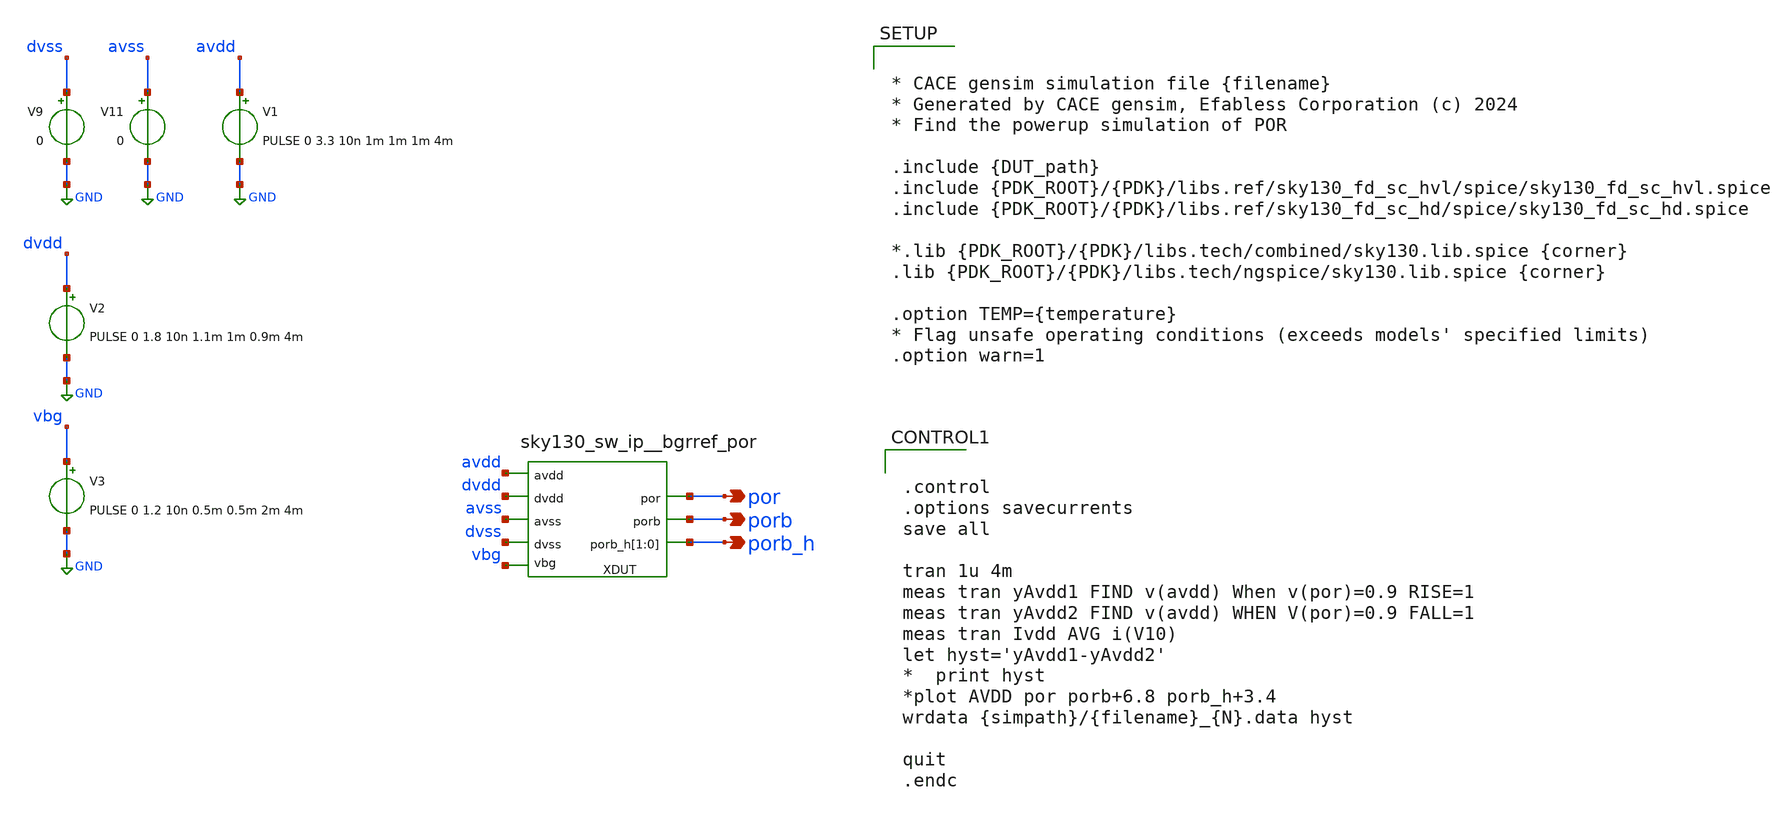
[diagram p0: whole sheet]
** sch_path: cace/templates/por_hys.sch
**.subckt por_hys por porb porb_h
*.opin por
*.opin porb
*.opin porb_h
XDUT vbg por avss avdd dvdd porb dvss porb_h porb_h sky130_sw_ip__bgrref_por
V9 dvss GND 0
V1 avdd GND PULSE 0 3.3 10n 1m 1m 1m 4m
V11 avss GND 0
V2 dvdd GND PULSE 0 1.8 10n 1.1m 1m 0.9m 4m
V3 vbg GND PULSE 0 1.2 10n 0.5m 0.5m 2m 4m
**** begin user architecture code


.control
.options savecurrents
save all

tran 1u 4m
meas tran yAvdd1 FIND v(avdd) When v(por)=0.9 RISE=1
meas tran yAvdd2 FIND v(avdd) WHEN V(por)=0.9 FALL=1
meas tran Ivdd AVG i(V10)
let hyst='yAvdd1-yAvdd2'
*  print hyst
*plot AVDD por porb+6.8 porb_h+3.4
wrdata {simpath}/{filename}_{N}.data hyst

quit
.endc




* CACE gensim simulation file {filename}
* Generated by CACE gensim, Efabless Corporation (c) 2024
* Find the powerup simulation of POR

.include {DUT_path}
.include {PDK_ROOT}/{PDK}/libs.ref/sky130_fd_sc_hvl/spice/sky130_fd_sc_hvl.spice
.include {PDK_ROOT}/{PDK}/libs.ref/sky130_fd_sc_hd/spice/sky130_fd_sc_hd.spice

*.lib {PDK_ROOT}/{PDK}/libs.tech/combined/sky130.lib.spice {corner}
.lib {PDK_ROOT}/{PDK}/libs.tech/ngspice/sky130.lib.spice {corner}

.option TEMP={temperature}
* Flag unsafe operating conditions (exceeds models' specified limits)
.option warn=1


**** end user architecture code
**.ends
.GLOBAL GND
.end
